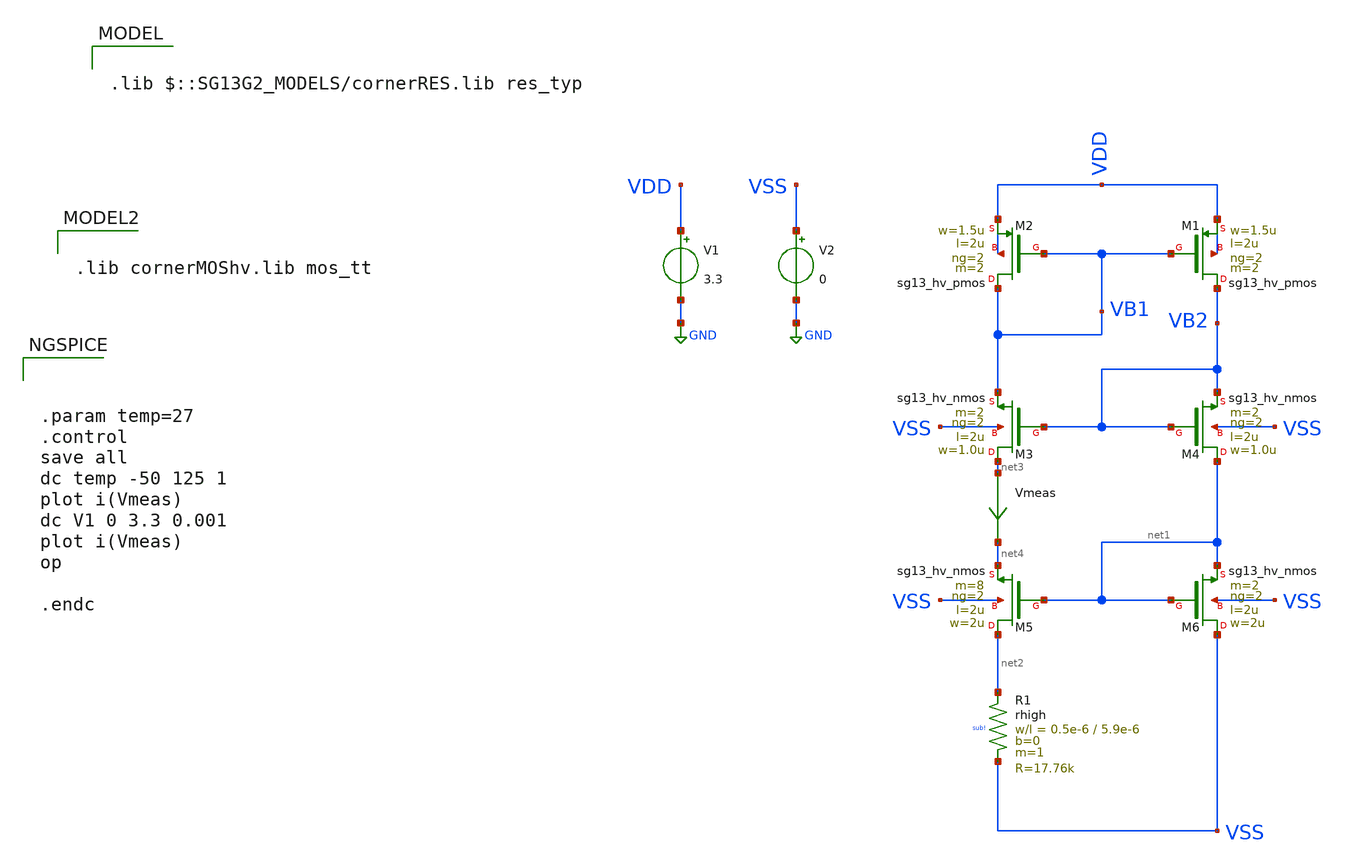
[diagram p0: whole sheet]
** sch_path: Learning/single_ended_amplifiers/Design_and_Analysis_of_Two-Stage_CMOS_Operational_Amplifier_for_Fluorescence_Signal_Processing_ihp130_3_3V/transcondutance/design.sch
**.subckt design
V1 VDD GND 3.3
V2 VSS GND 0
XM2 VB1 VB1 VDD VDD sg13_hv_pmos w=1.5u l=2u ng=2 m=2 mm_ok=1
XM1 VB2 VB1 VDD VDD sg13_hv_pmos w=1.5u l=2u ng=2 m=2 mm_ok=1
XM3 net3 VB2 VB1 VSS sg13_hv_nmos w=1.0u l=2u ng=2 m=2 mm_ok=1
XM4 net1 VB2 VB2 VSS sg13_hv_nmos w=1.0u l=2u ng=2 m=2 mm_ok=1
XM5 net2 net1 net4 VSS sg13_hv_nmos w=2u l=2u ng=2 m=8 mm_ok=1
XM6 VSS net1 net1 VSS sg13_hv_nmos w=2u l=2u ng=2 m=2 mm_ok=1
Vmeas net3 net4 0
.save i(vmeas)
XR1 net2 VSS sub! rhigh w=0.5e-6 l=5.9e-6 m=1 b=0 mm_ok=1
**** begin user architecture code

.lib $::SG13G2_MODELS/cornerRES.lib res_typ


.lib cornerMOShv.lib mos_tt

**** end user architecture code
**.ends
.GLOBAL GND
**** begin user architecture code



.param temp=27
.control
save all
dc temp -50 125 1
plot i(Vmeas)
dc V1 0 3.3 0.001
plot i(Vmeas)
op

.endc


**** end user architecture code
.end
